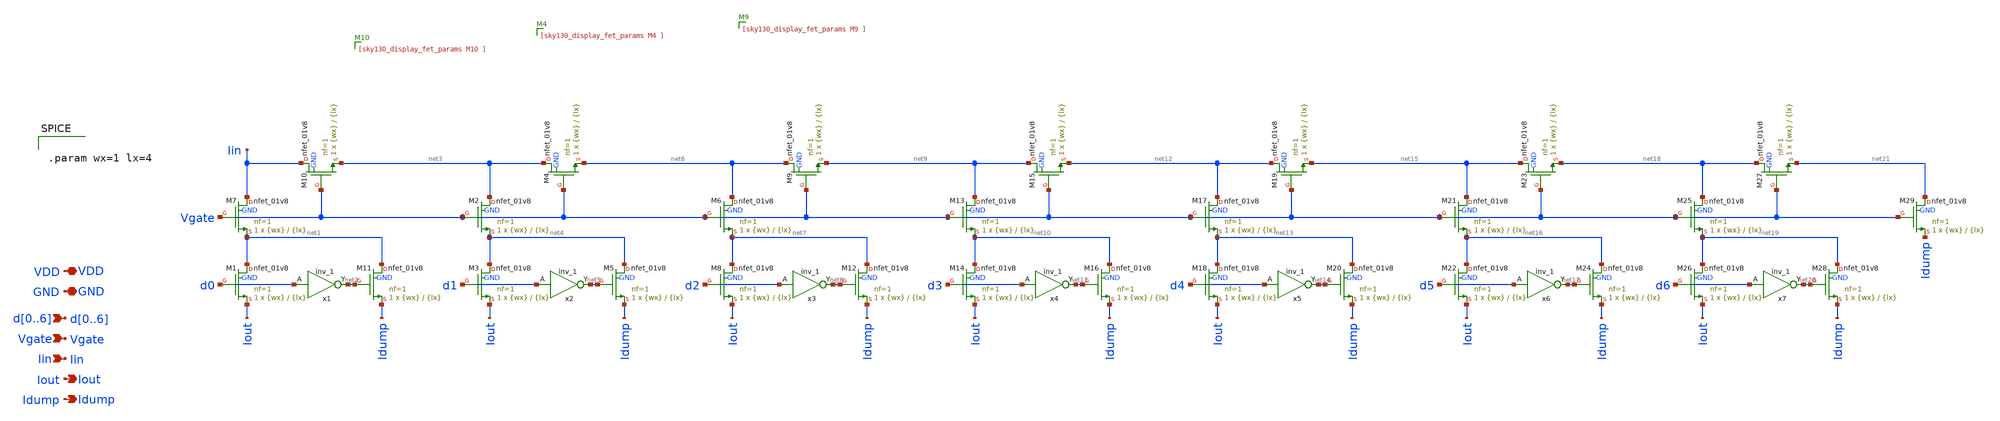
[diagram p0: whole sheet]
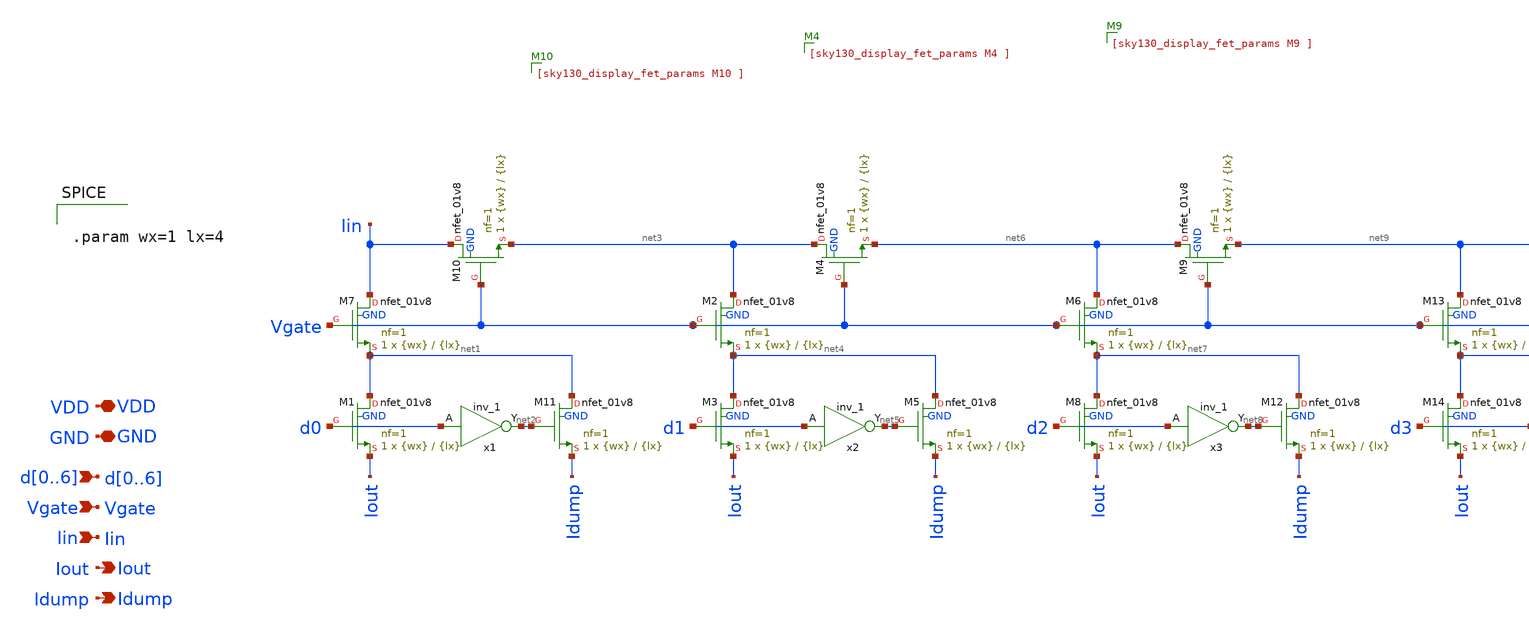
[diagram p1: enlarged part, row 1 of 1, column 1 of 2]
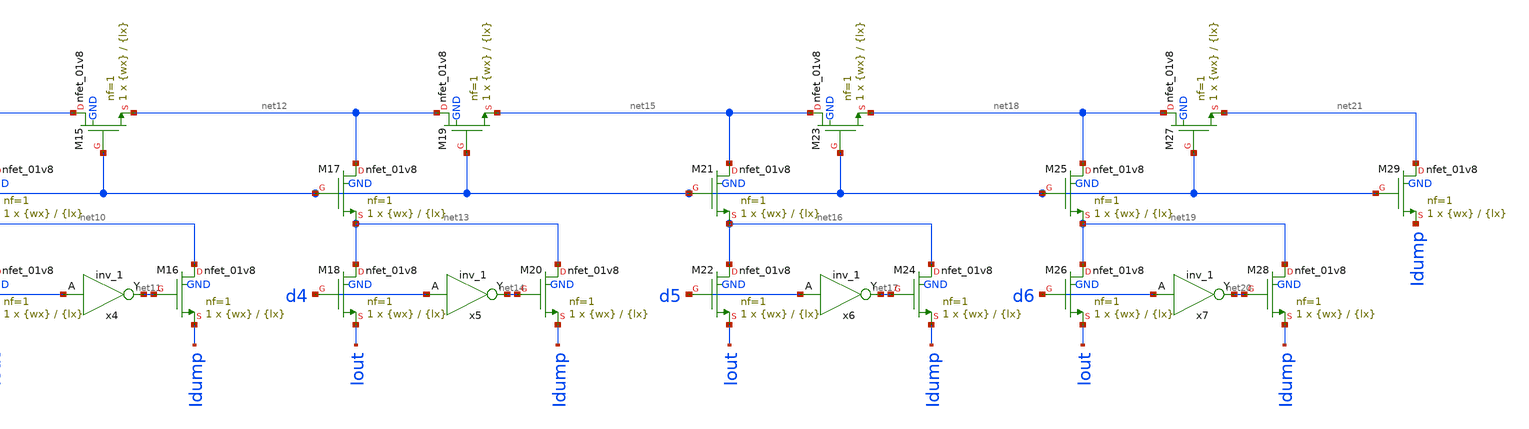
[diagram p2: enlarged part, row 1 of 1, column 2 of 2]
** sch_path: sch/ladder/ladder.sch
**.subckt ladder d0,d1,d2,d3,d4,d5,d6 Iout VDD GND Vgate Idump Iin
*.ipin d0,d1,d2,d3,d4,d5,d6
*.opin Iout
*.iopin VDD
*.iopin GND
*.ipin Vgate
*.opin Idump
*.ipin Iin
XM7 Iin Vgate net1 GND sky130_fd_pr__nfet_01v8 L={lx} W={wx} nf=1 ad='int((1 + 1)/2) * {wx} / 1 * 0.29'
+ as='int((1 + 2)/2) * {wx} / 1 * 0.29' pd='2*int((1 + 1)/2) * ({wx} / 1 + 0.29)' ps='2*int((1 + 2)/2) * ({wx} / 1 + 0.29)'
+ nrd='0.29 / {wx} ' nrs='0.29 / {wx} ' sa=0 sb=0 sd=0 mult=1 m=1
XM1 net1 d0 Iout GND sky130_fd_pr__nfet_01v8 L={lx} W={wx} nf=1 ad='int((1 + 1)/2) * {wx} / 1 * 0.29'
+ as='int((1 + 2)/2) * {wx} / 1 * 0.29' pd='2*int((1 + 1)/2) * ({wx} / 1 + 0.29)' ps='2*int((1 + 2)/2) * ({wx} / 1 + 0.29)'
+ nrd='0.29 / {wx} ' nrs='0.29 / {wx} ' sa=0 sb=0 sd=0 mult=1 m=1
XM10 Iin Vgate net3 GND sky130_fd_pr__nfet_01v8 L={lx} W={wx} nf=1 ad='int((1 + 1)/2) * {wx} / 1 * 0.29'
+ as='int((1 + 2)/2) * {wx} / 1 * 0.29' pd='2*int((1 + 1)/2) * ({wx} / 1 + 0.29)' ps='2*int((1 + 2)/2) * ({wx} / 1 + 0.29)'
+ nrd='0.29 / {wx} ' nrs='0.29 / {wx} ' sa=0 sb=0 sd=0 mult=1 m=1
x1 d0 GND GND VDD VDD net2 sky130_fd_sc_hd__inv_1
XM11 net1 net2 Idump GND sky130_fd_pr__nfet_01v8 L={lx} W={wx} nf=1 ad='int((1 + 1)/2) * {wx} / 1 * 0.29'
+ as='int((1 + 2)/2) * {wx} / 1 * 0.29' pd='2*int((1 + 1)/2) * ({wx} / 1 + 0.29)' ps='2*int((1 + 2)/2) * ({wx} / 1 + 0.29)'
+ nrd='0.29 / {wx} ' nrs='0.29 / {wx} ' sa=0 sb=0 sd=0 mult=1 m=1
XM2 net3 Vgate net4 GND sky130_fd_pr__nfet_01v8 L={lx} W={wx} nf=1 ad='int((1 + 1)/2) * {wx} / 1 * 0.29'
+ as='int((1 + 2)/2) * {wx} / 1 * 0.29' pd='2*int((1 + 1)/2) * ({wx} / 1 + 0.29)' ps='2*int((1 + 2)/2) * ({wx} / 1 + 0.29)'
+ nrd='0.29 / {wx} ' nrs='0.29 / {wx} ' sa=0 sb=0 sd=0 mult=1 m=1
XM3 net4 d1 Iout GND sky130_fd_pr__nfet_01v8 L={lx} W={wx} nf=1 ad='int((1 + 1)/2) * {wx} / 1 * 0.29'
+ as='int((1 + 2)/2) * {wx} / 1 * 0.29' pd='2*int((1 + 1)/2) * ({wx} / 1 + 0.29)' ps='2*int((1 + 2)/2) * ({wx} / 1 + 0.29)'
+ nrd='0.29 / {wx} ' nrs='0.29 / {wx} ' sa=0 sb=0 sd=0 mult=1 m=1
XM4 net3 Vgate net6 GND sky130_fd_pr__nfet_01v8 L={lx} W={wx} nf=1 ad='int((1 + 1)/2) * {wx} / 1 * 0.29'
+ as='int((1 + 2)/2) * {wx} / 1 * 0.29' pd='2*int((1 + 1)/2) * ({wx} / 1 + 0.29)' ps='2*int((1 + 2)/2) * ({wx} / 1 + 0.29)'
+ nrd='0.29 / {wx} ' nrs='0.29 / {wx} ' sa=0 sb=0 sd=0 mult=1 m=1
x2 d1 GND GND VDD VDD net5 sky130_fd_sc_hd__inv_1
XM5 net4 net5 Idump GND sky130_fd_pr__nfet_01v8 L={lx} W={wx} nf=1 ad='int((1 + 1)/2) * {wx} / 1 * 0.29'
+ as='int((1 + 2)/2) * {wx} / 1 * 0.29' pd='2*int((1 + 1)/2) * ({wx} / 1 + 0.29)' ps='2*int((1 + 2)/2) * ({wx} / 1 + 0.29)'
+ nrd='0.29 / {wx} ' nrs='0.29 / {wx} ' sa=0 sb=0 sd=0 mult=1 m=1
XM6 net6 Vgate net7 GND sky130_fd_pr__nfet_01v8 L={lx} W={wx} nf=1 ad='int((1 + 1)/2) * {wx} / 1 * 0.29'
+ as='int((1 + 2)/2) * {wx} / 1 * 0.29' pd='2*int((1 + 1)/2) * ({wx} / 1 + 0.29)' ps='2*int((1 + 2)/2) * ({wx} / 1 + 0.29)'
+ nrd='0.29 / {wx} ' nrs='0.29 / {wx} ' sa=0 sb=0 sd=0 mult=1 m=1
XM8 net7 d2 Iout GND sky130_fd_pr__nfet_01v8 L={lx} W={wx} nf=1 ad='int((1 + 1)/2) * {wx} / 1 * 0.29'
+ as='int((1 + 2)/2) * {wx} / 1 * 0.29' pd='2*int((1 + 1)/2) * ({wx} / 1 + 0.29)' ps='2*int((1 + 2)/2) * ({wx} / 1 + 0.29)'
+ nrd='0.29 / {wx} ' nrs='0.29 / {wx} ' sa=0 sb=0 sd=0 mult=1 m=1
XM9 net6 Vgate net9 GND sky130_fd_pr__nfet_01v8 L={lx} W={wx} nf=1 ad='int((1 + 1)/2) * {wx} / 1 * 0.29'
+ as='int((1 + 2)/2) * {wx} / 1 * 0.29' pd='2*int((1 + 1)/2) * ({wx} / 1 + 0.29)' ps='2*int((1 + 2)/2) * ({wx} / 1 + 0.29)'
+ nrd='0.29 / {wx} ' nrs='0.29 / {wx} ' sa=0 sb=0 sd=0 mult=1 m=1
x3 d2 GND GND VDD VDD net8 sky130_fd_sc_hd__inv_1
XM12 net7 net8 Idump GND sky130_fd_pr__nfet_01v8 L={lx} W={wx} nf=1 ad='int((1 + 1)/2) * {wx} / 1 * 0.29'
+ as='int((1 + 2)/2) * {wx} / 1 * 0.29' pd='2*int((1 + 1)/2) * ({wx} / 1 + 0.29)' ps='2*int((1 + 2)/2) * ({wx} / 1 + 0.29)'
+ nrd='0.29 / {wx} ' nrs='0.29 / {wx} ' sa=0 sb=0 sd=0 mult=1 m=1
XM13 net9 Vgate net10 GND sky130_fd_pr__nfet_01v8 L={lx} W={wx} nf=1 ad='int((1 + 1)/2) * {wx} / 1 * 0.29'
+ as='int((1 + 2)/2) * {wx} / 1 * 0.29' pd='2*int((1 + 1)/2) * ({wx} / 1 + 0.29)' ps='2*int((1 + 2)/2) * ({wx} / 1 + 0.29)'
+ nrd='0.29 / {wx} ' nrs='0.29 / {wx} ' sa=0 sb=0 sd=0 mult=1 m=1
XM14 net10 d3 Iout GND sky130_fd_pr__nfet_01v8 L={lx} W={wx} nf=1 ad='int((1 + 1)/2) * {wx} / 1 * 0.29'
+ as='int((1 + 2)/2) * {wx} / 1 * 0.29' pd='2*int((1 + 1)/2) * ({wx} / 1 + 0.29)' ps='2*int((1 + 2)/2) * ({wx} / 1 + 0.29)'
+ nrd='0.29 / {wx} ' nrs='0.29 / {wx} ' sa=0 sb=0 sd=0 mult=1 m=1
XM15 net9 Vgate net12 GND sky130_fd_pr__nfet_01v8 L={lx} W={wx} nf=1 ad='int((1 + 1)/2) * {wx} / 1 * 0.29'
+ as='int((1 + 2)/2) * {wx} / 1 * 0.29' pd='2*int((1 + 1)/2) * ({wx} / 1 + 0.29)' ps='2*int((1 + 2)/2) * ({wx} / 1 + 0.29)'
+ nrd='0.29 / {wx} ' nrs='0.29 / {wx} ' sa=0 sb=0 sd=0 mult=1 m=1
x4 d3 GND GND VDD VDD net11 sky130_fd_sc_hd__inv_1
XM16 net10 net11 Idump GND sky130_fd_pr__nfet_01v8 L={lx} W={wx} nf=1 ad='int((1 + 1)/2) * {wx} / 1 * 0.29'
+ as='int((1 + 2)/2) * {wx} / 1 * 0.29' pd='2*int((1 + 1)/2) * ({wx} / 1 + 0.29)' ps='2*int((1 + 2)/2) * ({wx} / 1 + 0.29)'
+ nrd='0.29 / {wx} ' nrs='0.29 / {wx} ' sa=0 sb=0 sd=0 mult=1 m=1
XM17 net12 Vgate net13 GND sky130_fd_pr__nfet_01v8 L={lx} W={wx} nf=1 ad='int((1 + 1)/2) * {wx} / 1 * 0.29'
+ as='int((1 + 2)/2) * {wx} / 1 * 0.29' pd='2*int((1 + 1)/2) * ({wx} / 1 + 0.29)' ps='2*int((1 + 2)/2) * ({wx} / 1 + 0.29)'
+ nrd='0.29 / {wx} ' nrs='0.29 / {wx} ' sa=0 sb=0 sd=0 mult=1 m=1
XM18 net13 d4 Iout GND sky130_fd_pr__nfet_01v8 L={lx} W={wx} nf=1 ad='int((1 + 1)/2) * {wx} / 1 * 0.29'
+ as='int((1 + 2)/2) * {wx} / 1 * 0.29' pd='2*int((1 + 1)/2) * ({wx} / 1 + 0.29)' ps='2*int((1 + 2)/2) * ({wx} / 1 + 0.29)'
+ nrd='0.29 / {wx} ' nrs='0.29 / {wx} ' sa=0 sb=0 sd=0 mult=1 m=1
XM19 net12 Vgate net15 GND sky130_fd_pr__nfet_01v8 L={lx} W={wx} nf=1 ad='int((1 + 1)/2) * {wx} / 1 * 0.29'
+ as='int((1 + 2)/2) * {wx} / 1 * 0.29' pd='2*int((1 + 1)/2) * ({wx} / 1 + 0.29)' ps='2*int((1 + 2)/2) * ({wx} / 1 + 0.29)'
+ nrd='0.29 / {wx} ' nrs='0.29 / {wx} ' sa=0 sb=0 sd=0 mult=1 m=1
x5 d4 GND GND VDD VDD net14 sky130_fd_sc_hd__inv_1
XM20 net13 net14 Idump GND sky130_fd_pr__nfet_01v8 L={lx} W={wx} nf=1 ad='int((1 + 1)/2) * {wx} / 1 * 0.29'
+ as='int((1 + 2)/2) * {wx} / 1 * 0.29' pd='2*int((1 + 1)/2) * ({wx} / 1 + 0.29)' ps='2*int((1 + 2)/2) * ({wx} / 1 + 0.29)'
+ nrd='0.29 / {wx} ' nrs='0.29 / {wx} ' sa=0 sb=0 sd=0 mult=1 m=1
XM21 net15 Vgate net16 GND sky130_fd_pr__nfet_01v8 L={lx} W={wx} nf=1 ad='int((1 + 1)/2) * {wx} / 1 * 0.29'
+ as='int((1 + 2)/2) * {wx} / 1 * 0.29' pd='2*int((1 + 1)/2) * ({wx} / 1 + 0.29)' ps='2*int((1 + 2)/2) * ({wx} / 1 + 0.29)'
+ nrd='0.29 / {wx} ' nrs='0.29 / {wx} ' sa=0 sb=0 sd=0 mult=1 m=1
XM22 net16 d5 Iout GND sky130_fd_pr__nfet_01v8 L={lx} W={wx} nf=1 ad='int((1 + 1)/2) * {wx} / 1 * 0.29'
+ as='int((1 + 2)/2) * {wx} / 1 * 0.29' pd='2*int((1 + 1)/2) * ({wx} / 1 + 0.29)' ps='2*int((1 + 2)/2) * ({wx} / 1 + 0.29)'
+ nrd='0.29 / {wx} ' nrs='0.29 / {wx} ' sa=0 sb=0 sd=0 mult=1 m=1
XM23 net15 Vgate net18 GND sky130_fd_pr__nfet_01v8 L={lx} W={wx} nf=1 ad='int((1 + 1)/2) * {wx} / 1 * 0.29'
+ as='int((1 + 2)/2) * {wx} / 1 * 0.29' pd='2*int((1 + 1)/2) * ({wx} / 1 + 0.29)' ps='2*int((1 + 2)/2) * ({wx} / 1 + 0.29)'
+ nrd='0.29 / {wx} ' nrs='0.29 / {wx} ' sa=0 sb=0 sd=0 mult=1 m=1
x6 d5 GND GND VDD VDD net17 sky130_fd_sc_hd__inv_1
XM24 net16 net17 Idump GND sky130_fd_pr__nfet_01v8 L={lx} W={wx} nf=1 ad='int((1 + 1)/2) * {wx} / 1 * 0.29'
+ as='int((1 + 2)/2) * {wx} / 1 * 0.29' pd='2*int((1 + 1)/2) * ({wx} / 1 + 0.29)' ps='2*int((1 + 2)/2) * ({wx} / 1 + 0.29)'
+ nrd='0.29 / {wx} ' nrs='0.29 / {wx} ' sa=0 sb=0 sd=0 mult=1 m=1
XM25 net18 Vgate net19 GND sky130_fd_pr__nfet_01v8 L={lx} W={wx} nf=1 ad='int((1 + 1)/2) * {wx} / 1 * 0.29'
+ as='int((1 + 2)/2) * {wx} / 1 * 0.29' pd='2*int((1 + 1)/2) * ({wx} / 1 + 0.29)' ps='2*int((1 + 2)/2) * ({wx} / 1 + 0.29)'
+ nrd='0.29 / {wx} ' nrs='0.29 / {wx} ' sa=0 sb=0 sd=0 mult=1 m=1
XM26 net19 d6 Iout GND sky130_fd_pr__nfet_01v8 L={lx} W={wx} nf=1 ad='int((1 + 1)/2) * {wx} / 1 * 0.29'
+ as='int((1 + 2)/2) * {wx} / 1 * 0.29' pd='2*int((1 + 1)/2) * ({wx} / 1 + 0.29)' ps='2*int((1 + 2)/2) * ({wx} / 1 + 0.29)'
+ nrd='0.29 / {wx} ' nrs='0.29 / {wx} ' sa=0 sb=0 sd=0 mult=1 m=1
XM27 net18 Vgate net21 GND sky130_fd_pr__nfet_01v8 L={lx} W={wx} nf=1 ad='int((1 + 1)/2) * {wx} / 1 * 0.29'
+ as='int((1 + 2)/2) * {wx} / 1 * 0.29' pd='2*int((1 + 1)/2) * ({wx} / 1 + 0.29)' ps='2*int((1 + 2)/2) * ({wx} / 1 + 0.29)'
+ nrd='0.29 / {wx} ' nrs='0.29 / {wx} ' sa=0 sb=0 sd=0 mult=1 m=1
x7 d6 GND GND VDD VDD net20 sky130_fd_sc_hd__inv_1
XM28 net19 net20 Idump GND sky130_fd_pr__nfet_01v8 L={lx} W={wx} nf=1 ad='int((1 + 1)/2) * {wx} / 1 * 0.29'
+ as='int((1 + 2)/2) * {wx} / 1 * 0.29' pd='2*int((1 + 1)/2) * ({wx} / 1 + 0.29)' ps='2*int((1 + 2)/2) * ({wx} / 1 + 0.29)'
+ nrd='0.29 / {wx} ' nrs='0.29 / {wx} ' sa=0 sb=0 sd=0 mult=1 m=1
XM29 net21 Vgate Idump GND sky130_fd_pr__nfet_01v8 L={lx} W={wx} nf=1 ad='int((1 + 1)/2) * {wx} / 1 * 0.29'
+ as='int((1 + 2)/2) * {wx} / 1 * 0.29' pd='2*int((1 + 1)/2) * ({wx} / 1 + 0.29)' ps='2*int((1 + 2)/2) * ({wx} / 1 + 0.29)'
+ nrd='0.29 / {wx} ' nrs='0.29 / {wx} ' sa=0 sb=0 sd=0 mult=1 m=1
**** begin user architecture code


.param wx=1 lx=4


**** end user architecture code
**.ends
.end
